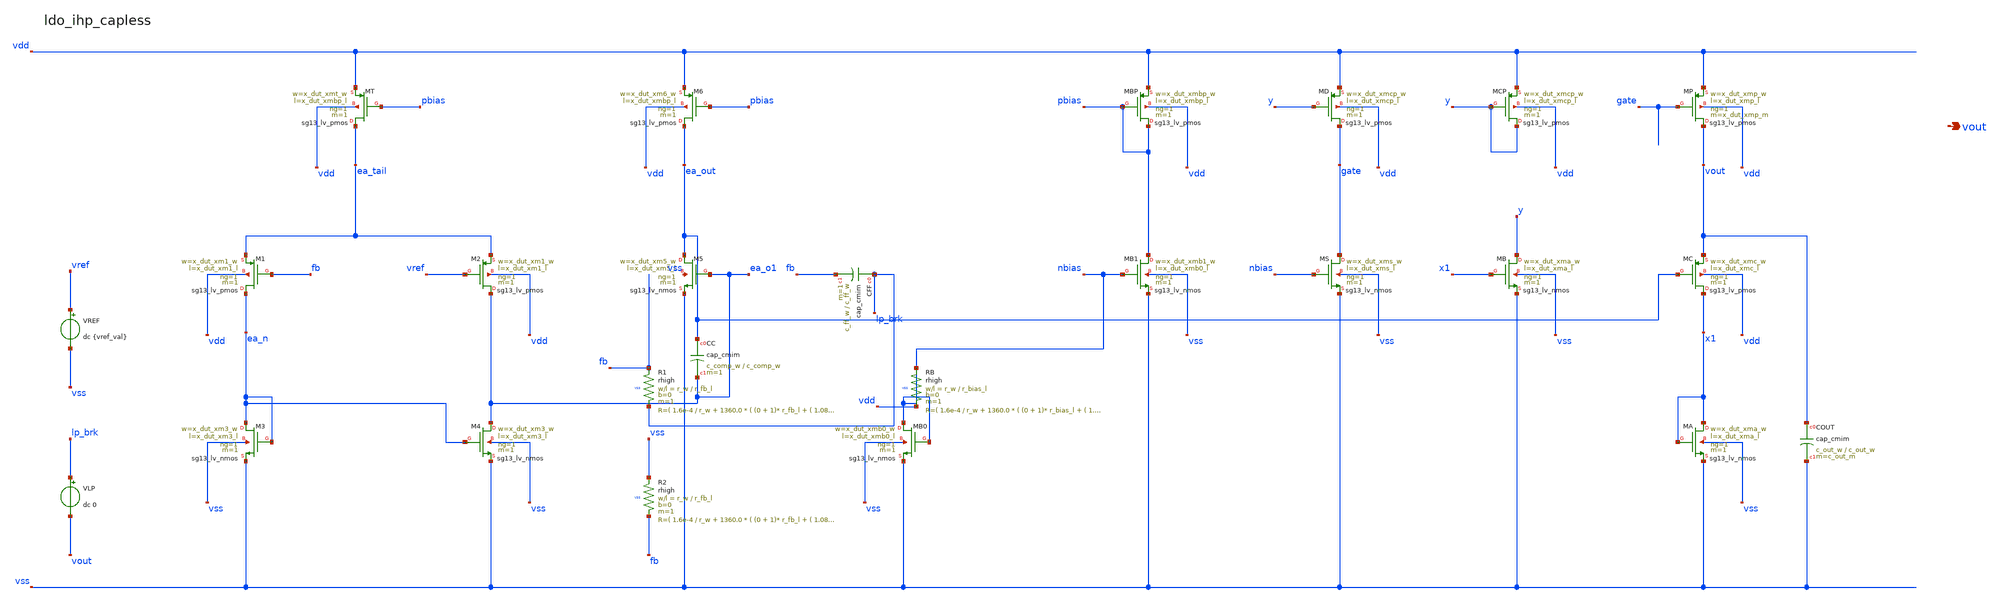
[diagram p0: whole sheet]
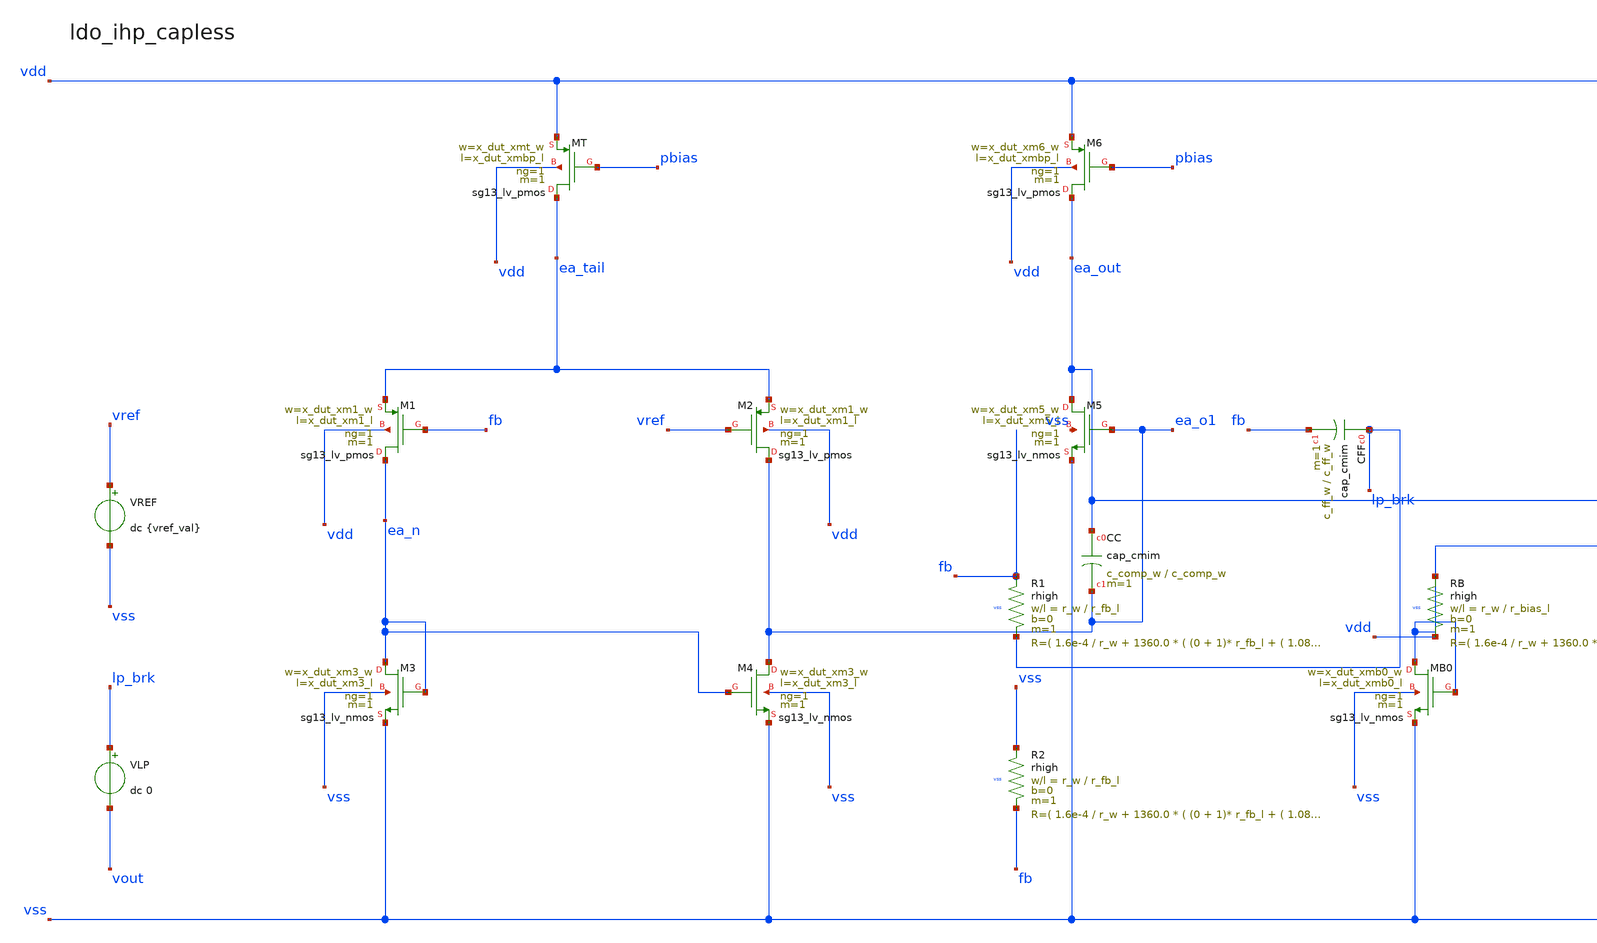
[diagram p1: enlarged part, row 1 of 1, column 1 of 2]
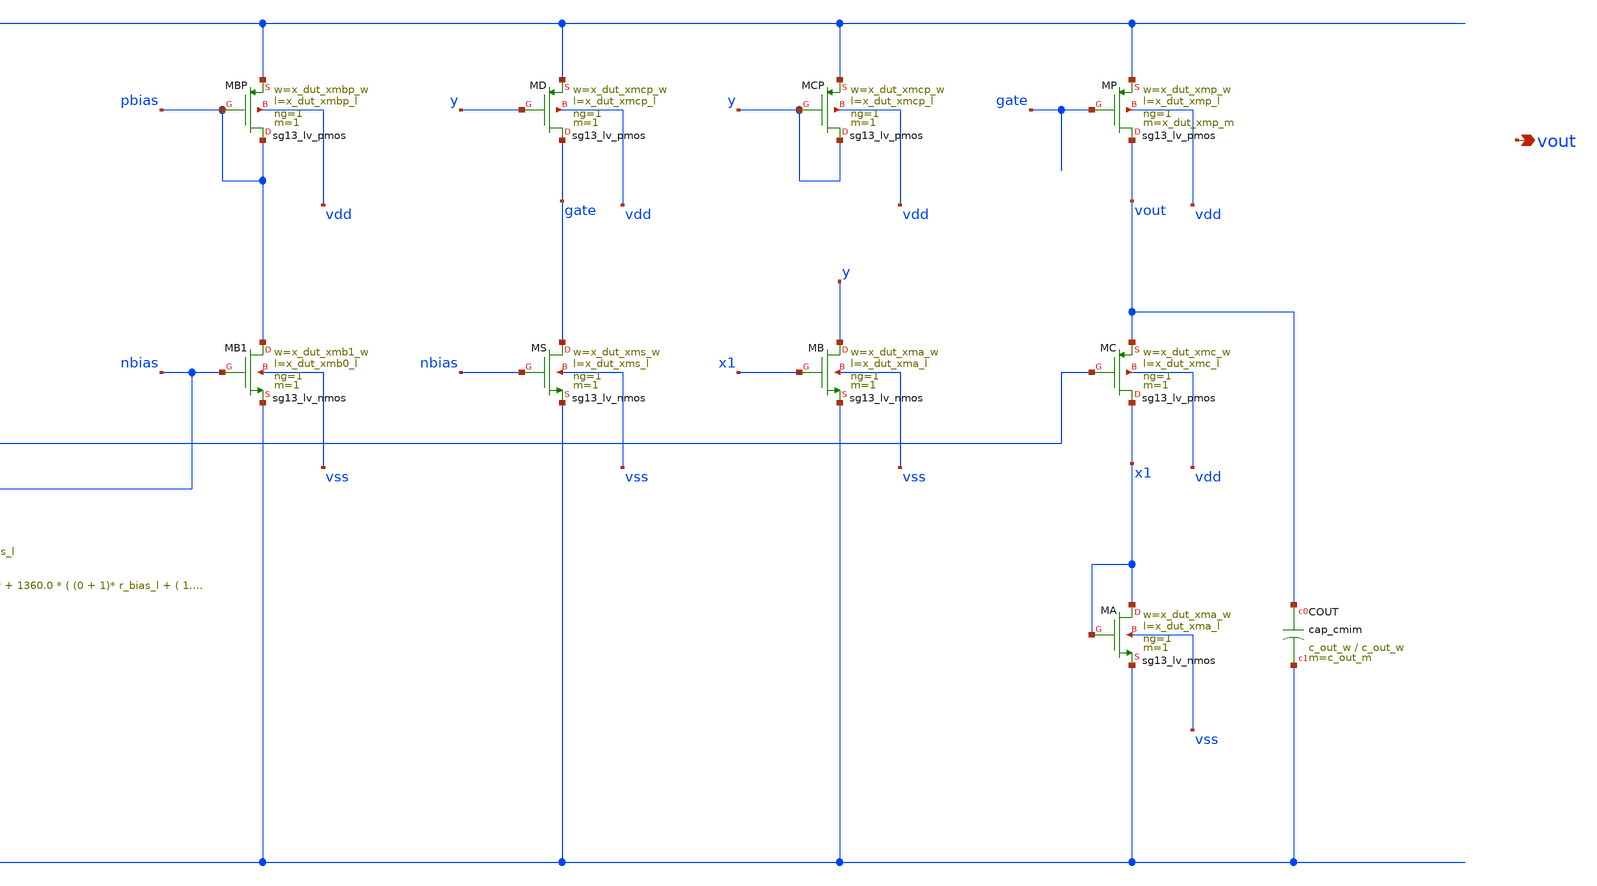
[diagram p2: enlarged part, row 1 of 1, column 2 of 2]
** sch_path: circuits/ldo_ihp_capless/xschem/ldo_ihp_capless_flat.sch
**.subckt ldo_ihp_capless_flat vout
*.opin vout
VREF vref vss dc {vref_val}
VLP lp_brk vout dc 0
XR1 fb lp_brk vss rhigh w=r_w l=r_fb_l m=1 b=0 mm_ok=1
XCFF lp_brk fb cap_cmim w=c_ff_w l=c_ff_w m=1 mm_ok=1
XR2 vss fb vss rhigh w=r_w l=r_fb_l m=1 b=0 mm_ok=1
XRB nbias vdd vss rhigh w=r_w l=r_bias_l m=1 b=0 mm_ok=1
XMB0 nbias nbias vss vss sg13_lv_nmos w=x_dut_xmb0_w l=x_dut_xmb0_l ng=1 m=1 mm_ok=1
XMB1 pbias nbias vss vss sg13_lv_nmos w=x_dut_xmb1_w l=x_dut_xmb0_l ng=1 m=1 mm_ok=1
XMBP pbias pbias vdd vdd sg13_lv_pmos w=x_dut_xmbp_w l=x_dut_xmbp_l ng=1 m=1 mm_ok=1
XMT ea_tail pbias vdd vdd sg13_lv_pmos w=x_dut_xmt_w l=x_dut_xmbp_l ng=1 m=1 mm_ok=1
XM1 ea_n fb ea_tail vdd sg13_lv_pmos w=x_dut_xm1_w l=x_dut_xm1_l ng=1 m=1 mm_ok=1
XM2 ea_o1 vref ea_tail vdd sg13_lv_pmos w=x_dut_xm1_w l=x_dut_xm1_l ng=1 m=1 mm_ok=1
XM3 ea_n ea_n vss vss sg13_lv_nmos w=x_dut_xm3_w l=x_dut_xm3_l ng=1 m=1 mm_ok=1
XM4 ea_o1 ea_n vss vss sg13_lv_nmos w=x_dut_xm3_w l=x_dut_xm3_l ng=1 m=1 mm_ok=1
XM5 ea_out ea_o1 vss vss sg13_lv_nmos w=x_dut_xm5_w l=x_dut_xm5_l ng=1 m=1 mm_ok=1
XM6 ea_out pbias vdd vdd sg13_lv_pmos w=x_dut_xm6_w l=x_dut_xmbp_l ng=1 m=1 mm_ok=1
XCC ea_out ea_o1 cap_cmim w=c_comp_w l=c_comp_w m=1 mm_ok=1
XMC x1 ea_out vout vdd sg13_lv_pmos w=x_dut_xmc_w l=x_dut_xmc_l ng=1 m=1 mm_ok=1
XMA x1 x1 vss vss sg13_lv_nmos w=x_dut_xma_w l=x_dut_xma_l ng=1 m=1 mm_ok=1
XMB y x1 vss vss sg13_lv_nmos w=x_dut_xma_w l=x_dut_xma_l ng=1 m=1 mm_ok=1
XMCP y y vdd vdd sg13_lv_pmos w=x_dut_xmcp_w l=x_dut_xmcp_l ng=1 m=1 mm_ok=1
XMD gate y vdd vdd sg13_lv_pmos w=x_dut_xmcp_w l=x_dut_xmcp_l ng=1 m=1 mm_ok=1
XMS gate nbias vss vss sg13_lv_nmos w=x_dut_xms_w l=x_dut_xms_l ng=1 m=1 mm_ok=1
XMP vout gate vdd vdd sg13_lv_pmos w=x_dut_xmp_w l=x_dut_xmp_l ng=1 m=x_dut_xmp_m mm_ok=1
XCOUT vout vss cap_cmim w=c_out_w l=c_out_w m=c_out_m mm_ok=1
**.ends
.end
